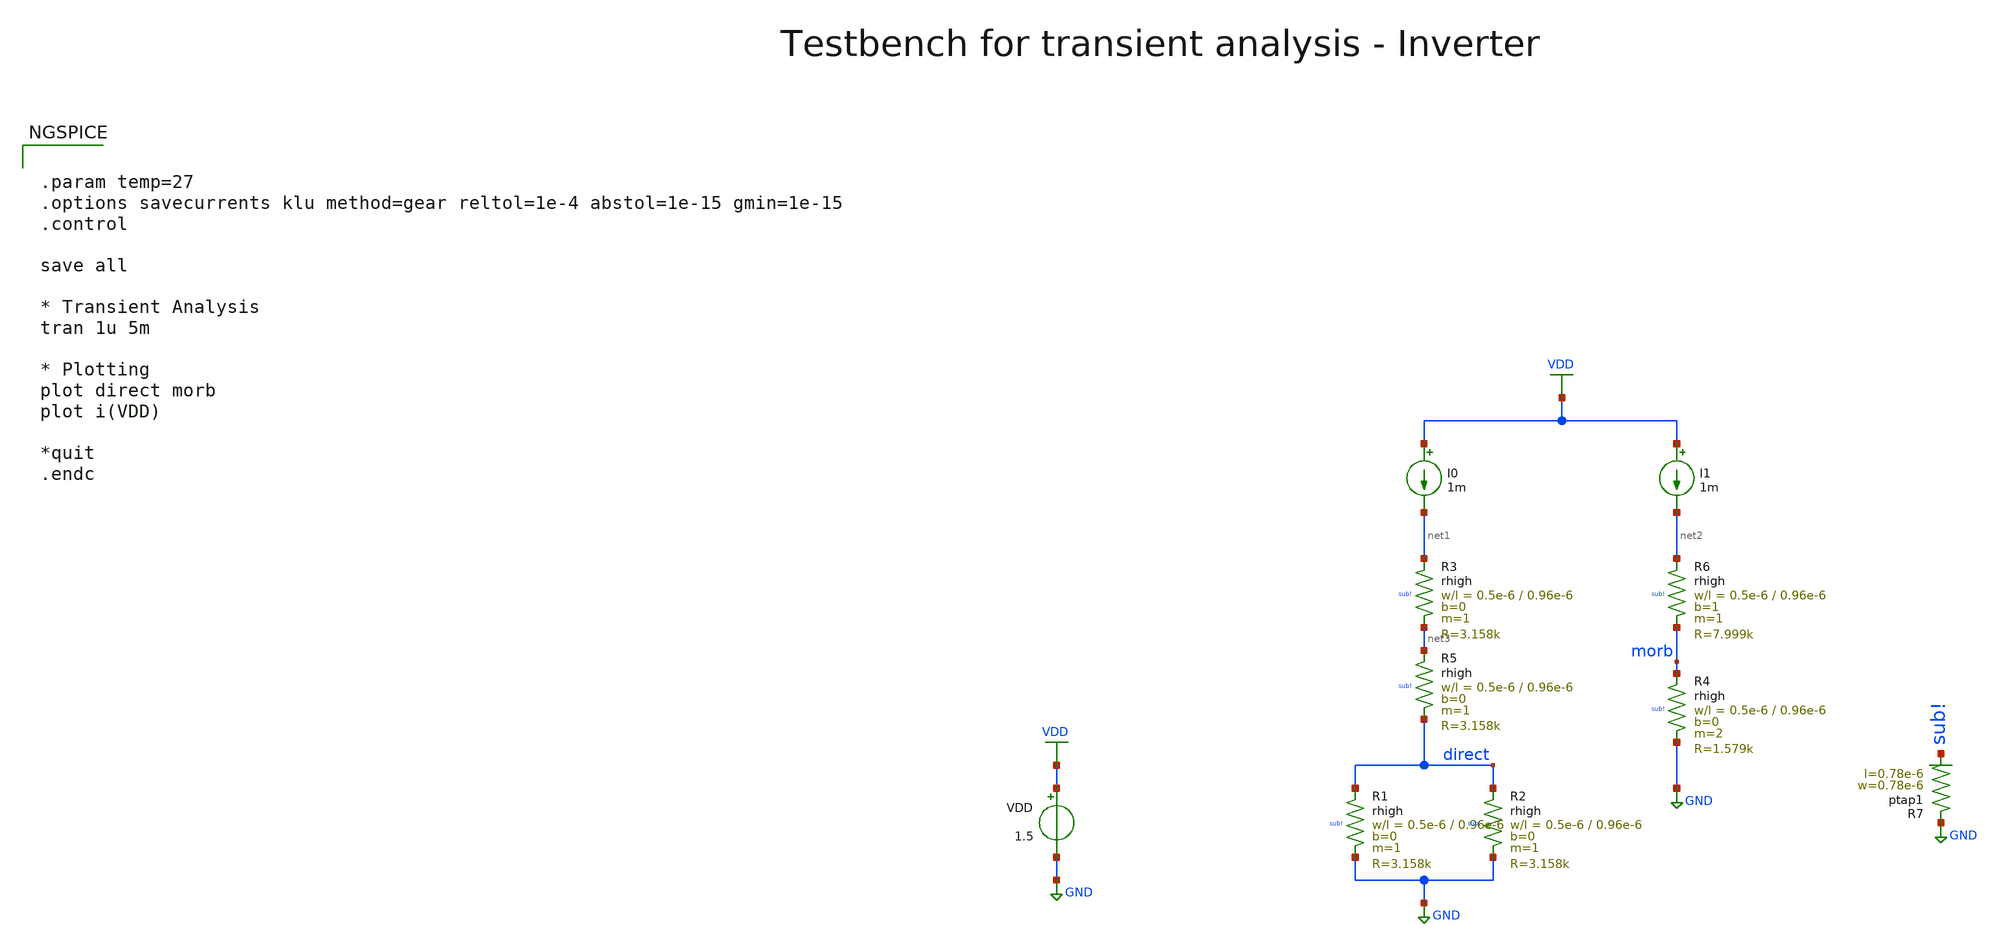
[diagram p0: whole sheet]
** sch_path: multiplier_support/testbench/rhigh_tb_tran.sch
**.subckt rhigh_tb_tran
VDD VDD GND 1.5
I0 VDD net1 1m
I1 VDD net2 1m
XR1 direct GND sub! rhigh w=0.5e-6 l=0.96e-6 m=1 b=0 mm_ok=1
XR2 direct GND sub! rhigh w=0.5e-6 l=0.96e-6 m=1 b=0 mm_ok=1
XR3 net1 net3 sub! rhigh w=0.5e-6 l=0.96e-6 m=1 b=0 mm_ok=1
XR4 morb GND sub! rhigh w=0.5e-6 l=0.96e-6 m=2 b=0 mm_ok=1
XR6 net2 morb sub! rhigh w=0.5e-6 l=0.96e-6 m=1 b=1 mm_ok=1
XR5 net3 direct sub! rhigh w=0.5e-6 l=0.96e-6 m=1 b=0 mm_ok=1
XR7 GND sub! ptap1 R=262.8 w=0.78e-6 l=0.78e-6
**** begin user architecture code


.param temp=27
.options savecurrents klu method=gear reltol=1e-4 abstol=1e-15 gmin=1e-15
.control

save all

* Transient Analysis
tran 1u 5m

* Plotting
plot direct morb
plot i(VDD)

*quit
.endc



.lib cornerMOSlv.lib mos_tt
.lib cornerMOShv.lib mos_tt
.lib cornerHBT.lib hbt_typ
.lib cornerRES.lib res_typ
.lib cornerCAP.lib cap_typ
.lib cornerDIO.lib dio_tt

**** end user architecture code
**.ends
.GLOBAL GND
.GLOBAL VDD
.end
